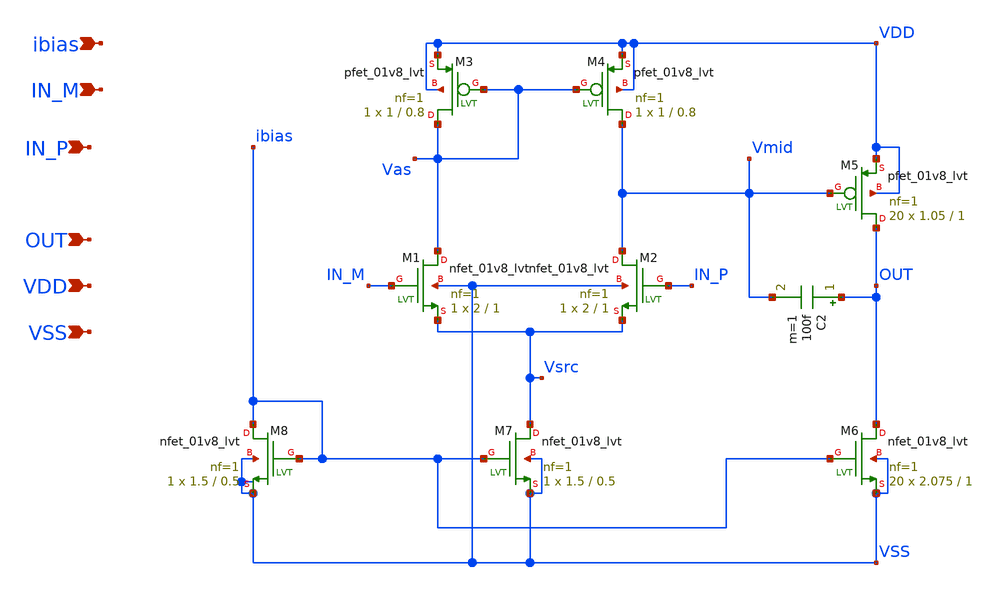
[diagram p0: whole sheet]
** sch_path: xchem/OTA3_jm.sch
**.subckt OTA3_jm IN_M IN_P OUT VDD VSS ibias
*.ipin IN_M
*.ipin IN_P
*.ipin OUT
*.ipin VDD
*.ipin VSS
*.ipin ibias
XM1 Vas IN_M Vsrc VSS sky130_fd_pr__nfet_01v8_lvt L=1 W=2 nf=1 ad='int((nf+1)/2) * W/nf * 0.29' as='int((nf+2)/2) * W/nf * 0.29'
+ pd='2*int((nf+1)/2) * (W/nf + 0.29)' ps='2*int((nf+2)/2) * (W/nf + 0.29)' nrd='0.29 / W' nrs='0.29 / W'
+ sa=0 sb=0 sd=0 mult=1 m=1
XM2 Vmid IN_P Vsrc VSS sky130_fd_pr__nfet_01v8_lvt L=1 W=2 nf=1 ad='int((nf+1)/2) * W/nf * 0.29' as='int((nf+2)/2) * W/nf * 0.29'
+ pd='2*int((nf+1)/2) * (W/nf + 0.29)' ps='2*int((nf+2)/2) * (W/nf + 0.29)' nrd='0.29 / W' nrs='0.29 / W'
+ sa=0 sb=0 sd=0 mult=1 m=1
XM3 Vas Vas VDD VDD sky130_fd_pr__pfet_01v8_lvt L=0.8 W=1 nf=1 ad='int((nf+1)/2) * W/nf * 0.29' as='int((nf+2)/2) * W/nf * 0.29'
+ pd='2*int((nf+1)/2) * (W/nf + 0.29)' ps='2*int((nf+2)/2) * (W/nf + 0.29)' nrd='0.29 / W' nrs='0.29 / W'
+ sa=0 sb=0 sd=0 mult=1 m=1
XM4 Vmid Vas VDD VDD sky130_fd_pr__pfet_01v8_lvt L=0.8 W=1 nf=1 ad='int((nf+1)/2) * W/nf * 0.29' as='int((nf+2)/2) * W/nf * 0.29'
+ pd='2*int((nf+1)/2) * (W/nf + 0.29)' ps='2*int((nf+2)/2) * (W/nf + 0.29)' nrd='0.29 / W' nrs='0.29 / W'
+ sa=0 sb=0 sd=0 mult=1 m=1
XM5 OUT Vmid VDD VDD sky130_fd_pr__pfet_01v8_lvt L=1 W=1.05 nf=1 ad='int((nf+1)/2) * W/nf * 0.29' as='int((nf+2)/2) * W/nf * 0.29'
+ pd='2*int((nf+1)/2) * (W/nf + 0.29)' ps='2*int((nf+2)/2) * (W/nf + 0.29)' nrd='0.29 / W' nrs='0.29 / W'
+ sa=0 sb=0 sd=0 mult=20 m=20
XM6 OUT ibias VSS VSS sky130_fd_pr__nfet_01v8_lvt L=1 W=2.075 nf=1 ad='int((nf+1)/2) * W/nf * 0.29' as='int((nf+2)/2) * W/nf * 0.29'
+ pd='2*int((nf+1)/2) * (W/nf + 0.29)' ps='2*int((nf+2)/2) * (W/nf + 0.29)' nrd='0.29 / W' nrs='0.29 / W'
+ sa=0 sb=0 sd=0 mult=20 m=20
XM7 Vsrc ibias VSS VSS sky130_fd_pr__nfet_01v8_lvt L=0.5 W=1.5 nf=1 ad='int((nf+1)/2) * W/nf * 0.29'
+ as='int((nf+2)/2) * W/nf * 0.29' pd='2*int((nf+1)/2) * (W/nf + 0.29)' ps='2*int((nf+2)/2) * (W/nf + 0.29)'
+ nrd='0.29 / W' nrs='0.29 / W' sa=0 sb=0 sd=0 mult=1 m=1
XM8 ibias ibias VSS VSS sky130_fd_pr__nfet_01v8_lvt L=0.5 W=1.5 nf=1 ad='int((nf+1)/2) * W/nf * 0.29'
+ as='int((nf+2)/2) * W/nf * 0.29' pd='2*int((nf+1)/2) * (W/nf + 0.29)' ps='2*int((nf+2)/2) * (W/nf + 0.29)'
+ nrd='0.29 / W' nrs='0.29 / W' sa=0 sb=0 sd=0 mult=1 m=1
C2 OUT Vmid 100f m=1
**.ends
.end
